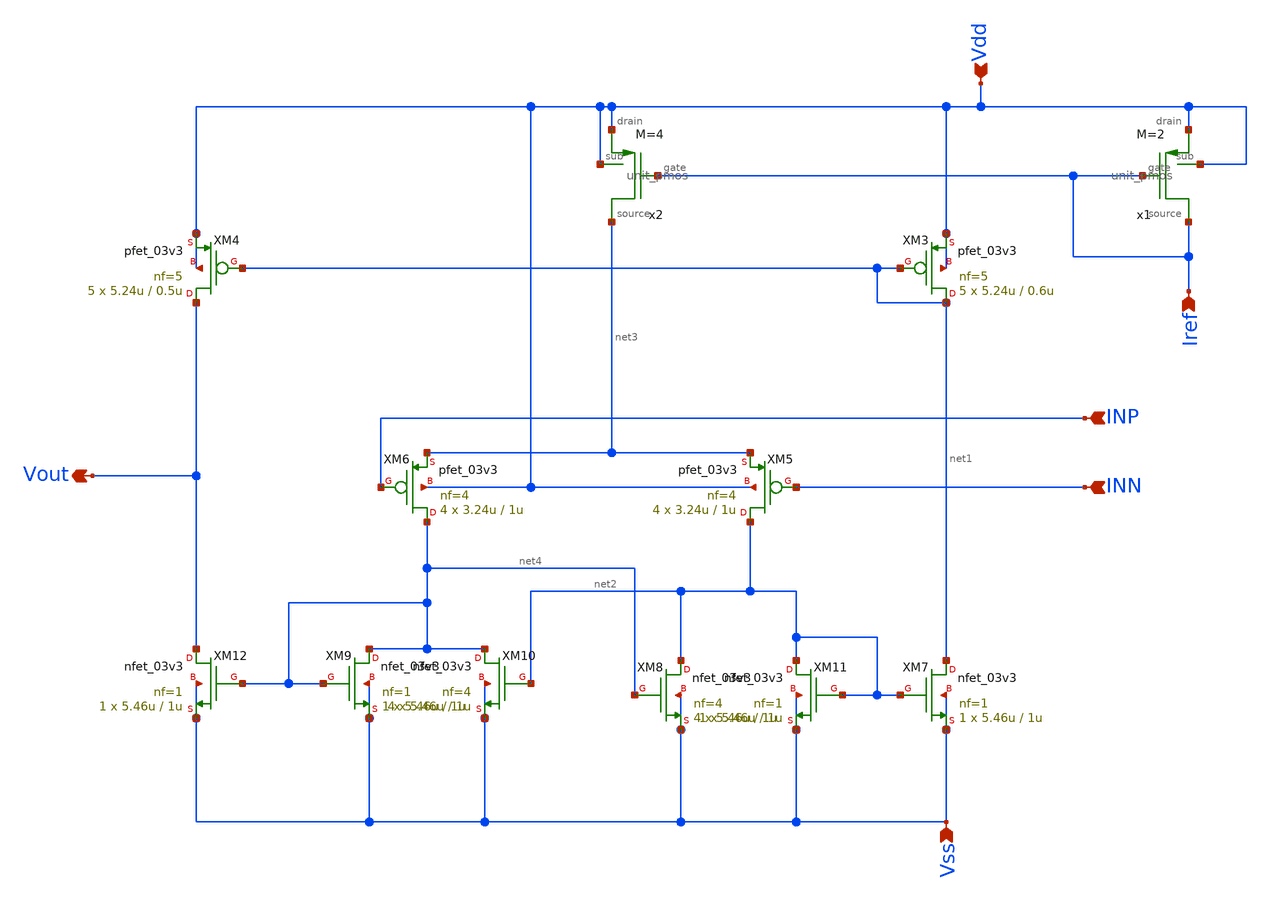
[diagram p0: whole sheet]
** sch_path: designs/libs/core_analog/Comparator/Pmos_Comparator.sch
**.subckt Pmos_Comparator Vdd Vss Iref INN INP Vout
*.ipin Vdd
*.ipin Vss
*.ipin Iref
*.ipin INN
*.ipin INP
*.opin Vout
XM3 net1 net1 Vdd Vdd pfet_03v3 L=0.6u W=5.24u nf=5 ad='int((nf+1)/2) * W/nf * 0.18u' as='int((nf+2)/2) * W/nf * 0.18u'
+ pd='2*int((nf+1)/2) * (W/nf + 0.18u)' ps='2*int((nf+2)/2) * (W/nf + 0.18u)' nrd='0.18u / W' nrs='0.18u / W'
+ sa=0 sb=0 sd=0 m=5
XM4 Vout net1 Vdd Vdd pfet_03v3 L=0.5u W=5.24u nf=5 ad='int((nf+1)/2) * W/nf * 0.18u' as='int((nf+2)/2) * W/nf * 0.18u'
+ pd='2*int((nf+1)/2) * (W/nf + 0.18u)' ps='2*int((nf+2)/2) * (W/nf + 0.18u)' nrd='0.18u / W' nrs='0.18u / W'
+ sa=0 sb=0 sd=0 m=5
XM5 net2 INN net3 Vdd pfet_03v3 L=1u W=3.24u nf=4 ad='int((nf+1)/2) * W/nf * 0.18u' as='int((nf+2)/2) * W/nf * 0.18u'
+ pd='2*int((nf+1)/2) * (W/nf + 0.18u)' ps='2*int((nf+2)/2) * (W/nf + 0.18u)' nrd='0.18u / W' nrs='0.18u / W'
+ sa=0 sb=0 sd=0 m=4
XM6 net4 INP net3 Vdd pfet_03v3 L=1u W=3.24u nf=4 ad='int((nf+1)/2) * W/nf * 0.18u' as='int((nf+2)/2) * W/nf * 0.18u'
+ pd='2*int((nf+1)/2) * (W/nf + 0.18u)' ps='2*int((nf+2)/2) * (W/nf + 0.18u)' nrd='0.18u / W' nrs='0.18u / W'
+ sa=0 sb=0 sd=0 m=4
XM7 net1 net2 Vss Vss nfet_03v3 L=1u W=5.46u nf=1 ad='int((nf+1)/2) * W/nf * 0.18u' as='int((nf+2)/2) * W/nf * 0.18u'
+ pd='2*int((nf+1)/2) * (W/nf + 0.18u)' ps='2*int((nf+2)/2) * (W/nf + 0.18u)' nrd='0.18u / W' nrs='0.18u / W'
+ sa=0 sb=0 sd=0 m=1
XM8 net2 net4 Vss Vss nfet_03v3 L=1u W=5.46u nf=4 ad='int((nf+1)/2) * W/nf * 0.18u' as='int((nf+2)/2) * W/nf * 0.18u'
+ pd='2*int((nf+1)/2) * (W/nf + 0.18u)' ps='2*int((nf+2)/2) * (W/nf + 0.18u)' nrd='0.18u / W' nrs='0.18u / W'
+ sa=0 sb=0 sd=0 m=4
XM9 net4 net4 Vss Vss nfet_03v3 L=1u W=5.46u nf=1 ad='int((nf+1)/2) * W/nf * 0.18u' as='int((nf+2)/2) * W/nf * 0.18u'
+ pd='2*int((nf+1)/2) * (W/nf + 0.18u)' ps='2*int((nf+2)/2) * (W/nf + 0.18u)' nrd='0.18u / W' nrs='0.18u / W'
+ sa=0 sb=0 sd=0 m=1
XM10 net4 net2 Vss Vss nfet_03v3 L=1u W=5.46u nf=4 ad='int((nf+1)/2) * W/nf * 0.18u' as='int((nf+2)/2) * W/nf * 0.18u'
+ pd='2*int((nf+1)/2) * (W/nf + 0.18u)' ps='2*int((nf+2)/2) * (W/nf + 0.18u)' nrd='0.18u / W' nrs='0.18u / W'
+ sa=0 sb=0 sd=0 m=4
XM11 net2 net2 Vss Vss nfet_03v3 L=1u W=5.46u nf=1 ad='int((nf+1)/2) * W/nf * 0.18u' as='int((nf+2)/2) * W/nf * 0.18u'
+ pd='2*int((nf+1)/2) * (W/nf + 0.18u)' ps='2*int((nf+2)/2) * (W/nf + 0.18u)' nrd='0.18u / W' nrs='0.18u / W'
+ sa=0 sb=0 sd=0 m=1
XM12 Vout net4 Vss Vss nfet_03v3 L=1u W=5.46u nf=1 ad='int((nf+1)/2) * W/nf * 0.18u' as='int((nf+2)/2) * W/nf * 0.18u'
+ pd='2*int((nf+1)/2) * (W/nf + 0.18u)' ps='2*int((nf+2)/2) * (W/nf + 0.18u)' nrd='0.18u / W' nrs='0.18u / W'
+ sa=0 sb=0 sd=0 m=1
x1 Vdd Vdd Iref Iref unit_pmos M=2
x2 Vdd Vdd Iref net3 unit_pmos M=4
**.ends

* expanding   symbol:  libs/core_analog/unit_pmos/unit_pmos.sym # of pins=4
** sym_path: libs/core_analog/unit_pmos/unit_pmos.sym
** sch_path: libs/core_analog/unit_pmos/unit_pmos.sch
.subckt unit_pmos drain sub gate source
*.iopin drain
*.iopin source
*.iopin sub
*.iopin gate
**** begin user architecture code

.param M=1

**** end user architecture code
XM3 drain gate source sub pfet_03v3 L=1u W=3.5u nf=1 ad='int((nf+1)/2) * W/nf * 0.18u' as='int((nf+2)/2) * W/nf * 0.18u'
+ pd='2*int((nf+1)/2) * (W/nf + 0.18u)' ps='2*int((nf+2)/2) * (W/nf + 0.18u)' nrd='0.18u / W' nrs='0.18u / W'
+ sa=0 sb=0 sd=0 m={M}
.ends

.end
